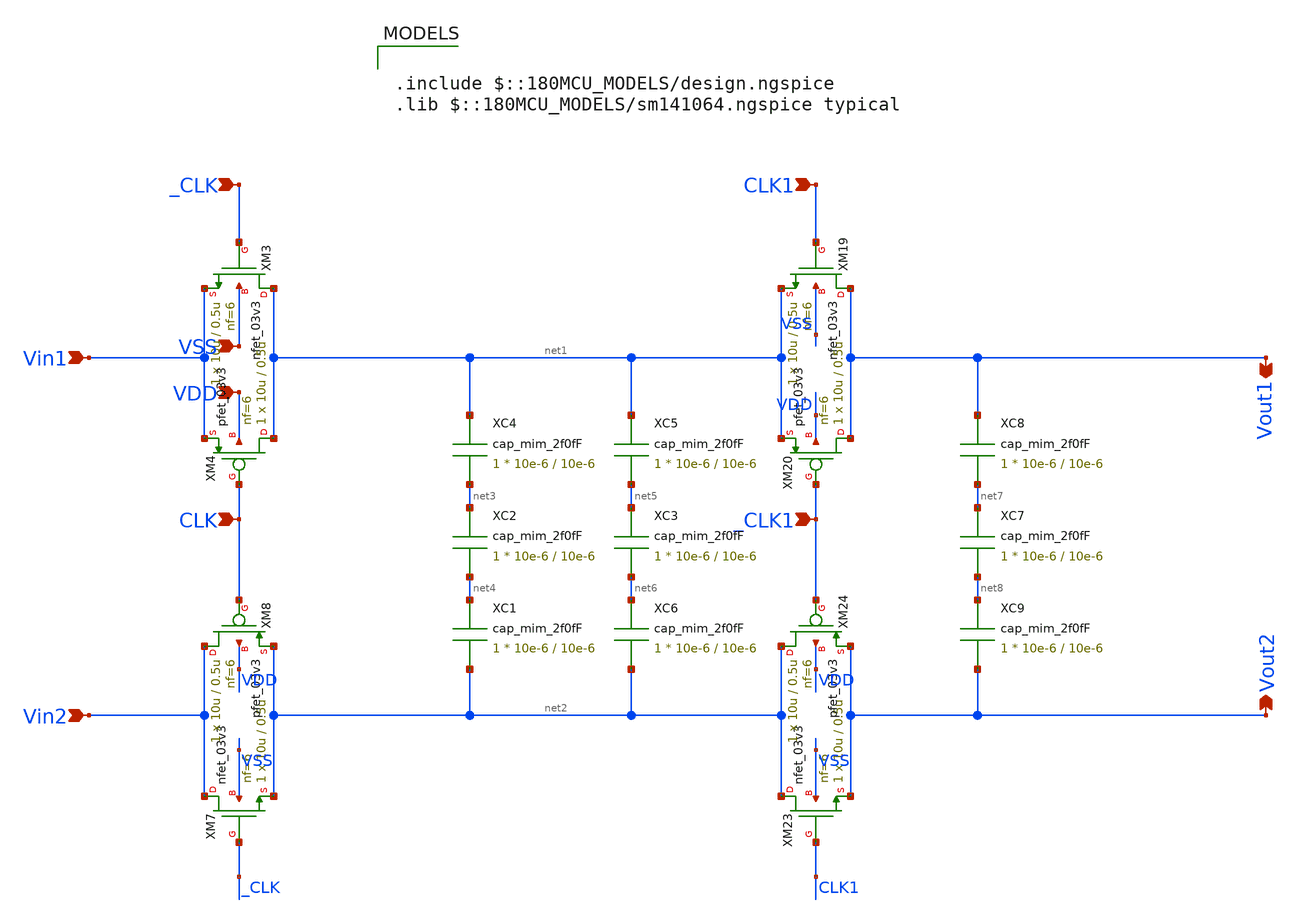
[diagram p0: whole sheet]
** sch_path: designs/libs/A2_core/top_lpf/lpf.sch
**.subckt lpf VSS VDD _CLK CLK Vin1 Vin2 CLK1 _CLK1 Vout1 Vout2
*.ipin VSS
*.ipin VDD
*.ipin _CLK
*.ipin CLK
*.ipin Vin1
*.ipin Vin2
*.ipin CLK1
*.ipin _CLK1
*.opin Vout1
*.opin Vout2
XM3 net1 _CLK Vin1 VSS nfet_03v3 L=0.5u W=10u nf=6 ad='int((nf+1)/2) * W/nf * 0.18u' as='int((nf+2)/2) * W/nf * 0.18u'
+ pd='2*int((nf+1)/2) * (W/nf + 0.18u)' ps='2*int((nf+2)/2) * (W/nf + 0.18u)' nrd='0.18u / W' nrs='0.18u / W'
+ sa=0 sb=0 sd=0 m=1
XM4 net1 CLK Vin1 VDD pfet_03v3 L=0.5u W=10u nf=6 ad='int((nf+1)/2) * W/nf * 0.18u' as='int((nf+2)/2) * W/nf * 0.18u'
+ pd='2*int((nf+1)/2) * (W/nf + 0.18u)' ps='2*int((nf+2)/2) * (W/nf + 0.18u)' nrd='0.18u / W' nrs='0.18u / W'
+ sa=0 sb=0 sd=0 m=1
XM7 Vin2 _CLK net2 VSS nfet_03v3 L=0.5u W=10u nf=6 ad='int((nf+1)/2) * W/nf * 0.18u' as='int((nf+2)/2) * W/nf * 0.18u'
+ pd='2*int((nf+1)/2) * (W/nf + 0.18u)' ps='2*int((nf+2)/2) * (W/nf + 0.18u)' nrd='0.18u / W' nrs='0.18u / W'
+ sa=0 sb=0 sd=0 m=1
XM8 Vin2 CLK net2 VDD pfet_03v3 L=0.5u W=10u nf=6 ad='int((nf+1)/2) * W/nf * 0.18u' as='int((nf+2)/2) * W/nf * 0.18u'
+ pd='2*int((nf+1)/2) * (W/nf + 0.18u)' ps='2*int((nf+2)/2) * (W/nf + 0.18u)' nrd='0.18u / W' nrs='0.18u / W'
+ sa=0 sb=0 sd=0 m=1
XM19 Vout1 CLK1 net1 VSS nfet_03v3 L=0.5u W=10u nf=6 ad='int((nf+1)/2) * W/nf * 0.18u' as='int((nf+2)/2) * W/nf * 0.18u'
+ pd='2*int((nf+1)/2) * (W/nf + 0.18u)' ps='2*int((nf+2)/2) * (W/nf + 0.18u)' nrd='0.18u / W' nrs='0.18u / W'
+ sa=0 sb=0 sd=0 m=1
XM20 Vout1 _CLK1 net1 VDD pfet_03v3 L=0.5u W=10u nf=6 ad='int((nf+1)/2) * W/nf * 0.18u' as='int((nf+2)/2) * W/nf * 0.18u'
+ pd='2*int((nf+1)/2) * (W/nf + 0.18u)' ps='2*int((nf+2)/2) * (W/nf + 0.18u)' nrd='0.18u / W' nrs='0.18u / W'
+ sa=0 sb=0 sd=0 m=1
XM23 net2 CLK1 Vout2 VSS nfet_03v3 L=0.5u W=10u nf=6 ad='int((nf+1)/2) * W/nf * 0.18u' as='int((nf+2)/2) * W/nf * 0.18u'
+ pd='2*int((nf+1)/2) * (W/nf + 0.18u)' ps='2*int((nf+2)/2) * (W/nf + 0.18u)' nrd='0.18u / W' nrs='0.18u / W'
+ sa=0 sb=0 sd=0 m=1
XM24 net2 _CLK1 Vout2 VDD pfet_03v3 L=0.5u W=10u nf=6 ad='int((nf+1)/2) * W/nf * 0.18u' as='int((nf+2)/2) * W/nf * 0.18u'
+ pd='2*int((nf+1)/2) * (W/nf + 0.18u)' ps='2*int((nf+2)/2) * (W/nf + 0.18u)' nrd='0.18u / W' nrs='0.18u / W'
+ sa=0 sb=0 sd=0 m=1
XC2 net3 net4 cap_mim_2f0fF c_width=10e-6 c_length=10e-6 m=1
XC4 net1 net3 cap_mim_2f0fF c_width=10e-6 c_length=10e-6 m=1
XC1 net4 net2 cap_mim_2f0fF c_width=10e-6 c_length=10e-6 m=1
XC3 net5 net6 cap_mim_2f0fF c_width=10e-6 c_length=10e-6 m=1
XC5 net1 net5 cap_mim_2f0fF c_width=10e-6 c_length=10e-6 m=1
XC6 net6 net2 cap_mim_2f0fF c_width=10e-6 c_length=10e-6 m=1
XC7 net7 net8 cap_mim_2f0fF c_width=10e-6 c_length=10e-6 m=1
XC8 Vout1 net7 cap_mim_2f0fF c_width=10e-6 c_length=10e-6 m=1
XC9 net8 Vout2 cap_mim_2f0fF c_width=10e-6 c_length=10e-6 m=1
**** begin user architecture code

.include $::180MCU_MODELS/design.ngspice
.lib $::180MCU_MODELS/sm141064.ngspice typical

**** end user architecture code
**.ends
.end
